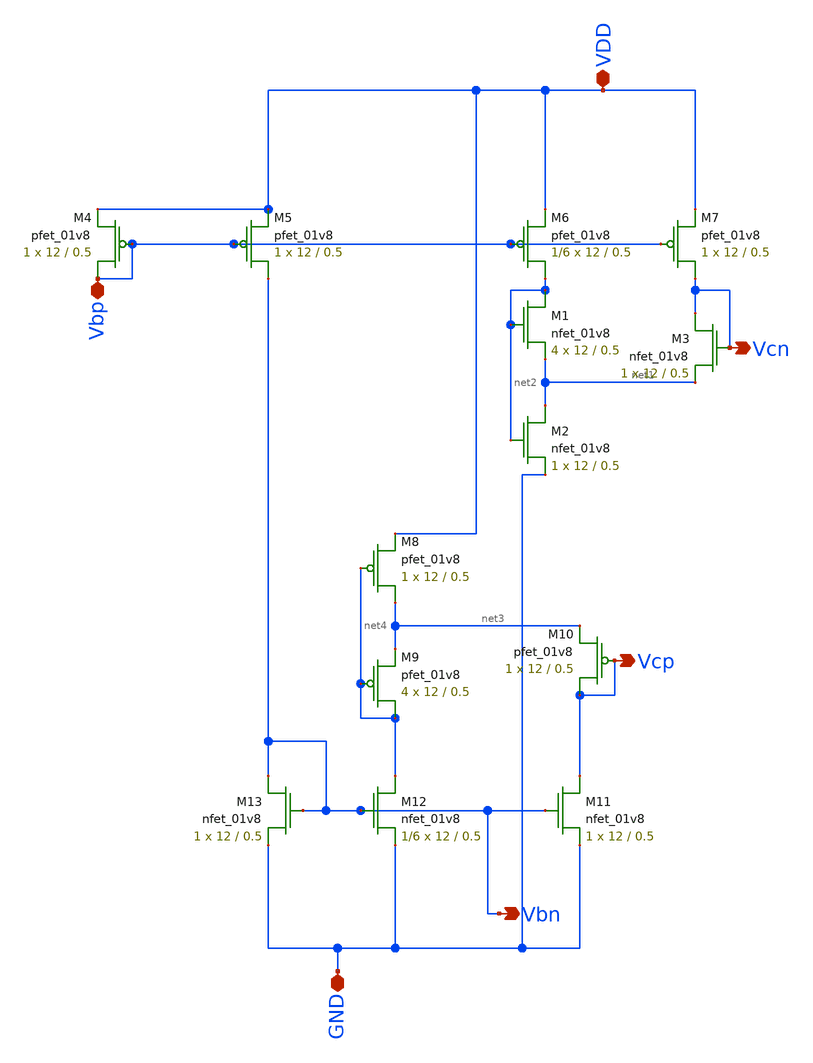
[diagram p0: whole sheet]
** sch_path: Miniproject3/Bias/Cascode_bias_voltage_generator.sch
**.subckt Cascode_bias_voltage_generator Vcp Vcn Vbn VDD GND Vbp
*.opin Vcp
*.opin Vcn
*.opin Vbn
*.iopin VDD
*.iopin GND
*.iopin Vbp
XM5 Vbn Vbp VDD VDD sky130_fd_pr__pfet_01v8 L=0.5 W=12 nf=1 ad='int((nf+1)/2) * W/nf * 0.29' as='int((nf+2)/2) * W/nf * 0.29'
+ pd='2*int((nf+1)/2) * (W/nf + 0.29)' ps='2*int((nf+2)/2) * (W/nf + 0.29)' nrd='0.29 / W' nrs='0.29 / W'
+ sa=0 sb=0 sd=0 mult=1 m=1
XM6 net2 Vbp VDD VDD sky130_fd_pr__pfet_01v8 L=0.5 W=12 nf=1 ad='int((nf+1)/2) * W/nf * 0.29' as='int((nf+2)/2) * W/nf * 0.29'
+ pd='2*int((nf+1)/2) * (W/nf + 0.29)' ps='2*int((nf+2)/2) * (W/nf + 0.29)' nrd='0.29 / W' nrs='0.29 / W'
+ sa=0 sb=0 sd=0 mult=1/6 m=1/6
XM7 Vcn Vbp VDD VDD sky130_fd_pr__pfet_01v8 L=0.5 W=12 nf=1 ad='int((nf+1)/2) * W/nf * 0.29' as='int((nf+2)/2) * W/nf * 0.29'
+ pd='2*int((nf+1)/2) * (W/nf + 0.29)' ps='2*int((nf+2)/2) * (W/nf + 0.29)' nrd='0.29 / W' nrs='0.29 / W'
+ sa=0 sb=0 sd=0 mult=1 m=1
XM8 net3 net4 VDD VDD sky130_fd_pr__pfet_01v8 L=0.5 W=12 nf=1 ad='int((nf+1)/2) * W/nf * 0.29' as='int((nf+2)/2) * W/nf * 0.29'
+ pd='2*int((nf+1)/2) * (W/nf + 0.29)' ps='2*int((nf+2)/2) * (W/nf + 0.29)' nrd='0.29 / W' nrs='0.29 / W'
+ sa=0 sb=0 sd=0 mult=1 m=1
XM9 net4 net4 net3 VDD sky130_fd_pr__pfet_01v8 L=0.5 W=12 nf=1 ad='int((nf+1)/2) * W/nf * 0.29' as='int((nf+2)/2) * W/nf * 0.29'
+ pd='2*int((nf+1)/2) * (W/nf + 0.29)' ps='2*int((nf+2)/2) * (W/nf + 0.29)' nrd='0.29 / W' nrs='0.29 / W'
+ sa=0 sb=0 sd=0 mult=4 m=4
XM10 Vcp Vcp net3 VDD sky130_fd_pr__pfet_01v8 L=0.5 W=12 nf=1 ad='int((nf+1)/2) * W/nf * 0.29' as='int((nf+2)/2) * W/nf * 0.29'
+ pd='2*int((nf+1)/2) * (W/nf + 0.29)' ps='2*int((nf+2)/2) * (W/nf + 0.29)' nrd='0.29 / W' nrs='0.29 / W'
+ sa=0 sb=0 sd=0 mult=1 m=1
XM11 Vcp Vbn GND GND sky130_fd_pr__nfet_01v8 L=0.5 W=12 nf=1 ad='int((nf+1)/2) * W/nf * 0.29' as='int((nf+2)/2) * W/nf * 0.29'
+ pd='2*int((nf+1)/2) * (W/nf + 0.29)' ps='2*int((nf+2)/2) * (W/nf + 0.29)' nrd='0.29 / W' nrs='0.29 / W'
+ sa=0 sb=0 sd=0 mult=1 m=1
XM12 net4 Vbn GND GND sky130_fd_pr__nfet_01v8 L=0.5 W=12 nf=1 ad='int((nf+1)/2) * W/nf * 0.29' as='int((nf+2)/2) * W/nf * 0.29'
+ pd='2*int((nf+1)/2) * (W/nf + 0.29)' ps='2*int((nf+2)/2) * (W/nf + 0.29)' nrd='0.29 / W' nrs='0.29 / W'
+ sa=0 sb=0 sd=0 mult=1/6 m=1/6
XM13 Vbn Vbn GND GND sky130_fd_pr__nfet_01v8 L=0.5 W=12 nf=1 ad='int((nf+1)/2) * W/nf * 0.29' as='int((nf+2)/2) * W/nf * 0.29'
+ pd='2*int((nf+1)/2) * (W/nf + 0.29)' ps='2*int((nf+2)/2) * (W/nf + 0.29)' nrd='0.29 / W' nrs='0.29 / W'
+ sa=0 sb=0 sd=0 mult=1 m=1
XM2 net1 net2 GND GND sky130_fd_pr__nfet_01v8 L=0.5 W=12 nf=1 ad='int((nf+1)/2) * W/nf * 0.29' as='int((nf+2)/2) * W/nf * 0.29'
+ pd='2*int((nf+1)/2) * (W/nf + 0.29)' ps='2*int((nf+2)/2) * (W/nf + 0.29)' nrd='0.29 / W' nrs='0.29 / W'
+ sa=0 sb=0 sd=0 mult=1 m=1
XM1 net2 net2 net1 GND sky130_fd_pr__nfet_01v8 L=0.5 W=12 nf=1 ad='int((nf+1)/2) * W/nf * 0.29' as='int((nf+2)/2) * W/nf * 0.29'
+ pd='2*int((nf+1)/2) * (W/nf + 0.29)' ps='2*int((nf+2)/2) * (W/nf + 0.29)' nrd='0.29 / W' nrs='0.29 / W'
+ sa=0 sb=0 sd=0 mult=4 m=4
XM3 Vcn Vcn net1 GND sky130_fd_pr__nfet_01v8 L=0.5 W=12 nf=1 ad='int((nf+1)/2) * W/nf * 0.29' as='int((nf+2)/2) * W/nf * 0.29'
+ pd='2*int((nf+1)/2) * (W/nf + 0.29)' ps='2*int((nf+2)/2) * (W/nf + 0.29)' nrd='0.29 / W' nrs='0.29 / W'
+ sa=0 sb=0 sd=0 mult=1 m=1
XM4 Vbp Vbp VDD VDD sky130_fd_pr__pfet_01v8 L=0.5 W=12 nf=1 ad='int((nf+1)/2) * W/nf * 0.29' as='int((nf+2)/2) * W/nf * 0.29'
+ pd='2*int((nf+1)/2) * (W/nf + 0.29)' ps='2*int((nf+2)/2) * (W/nf + 0.29)' nrd='0.29 / W' nrs='0.29 / W'
+ sa=0 sb=0 sd=0 mult=1 m=1
**.ends
.end
